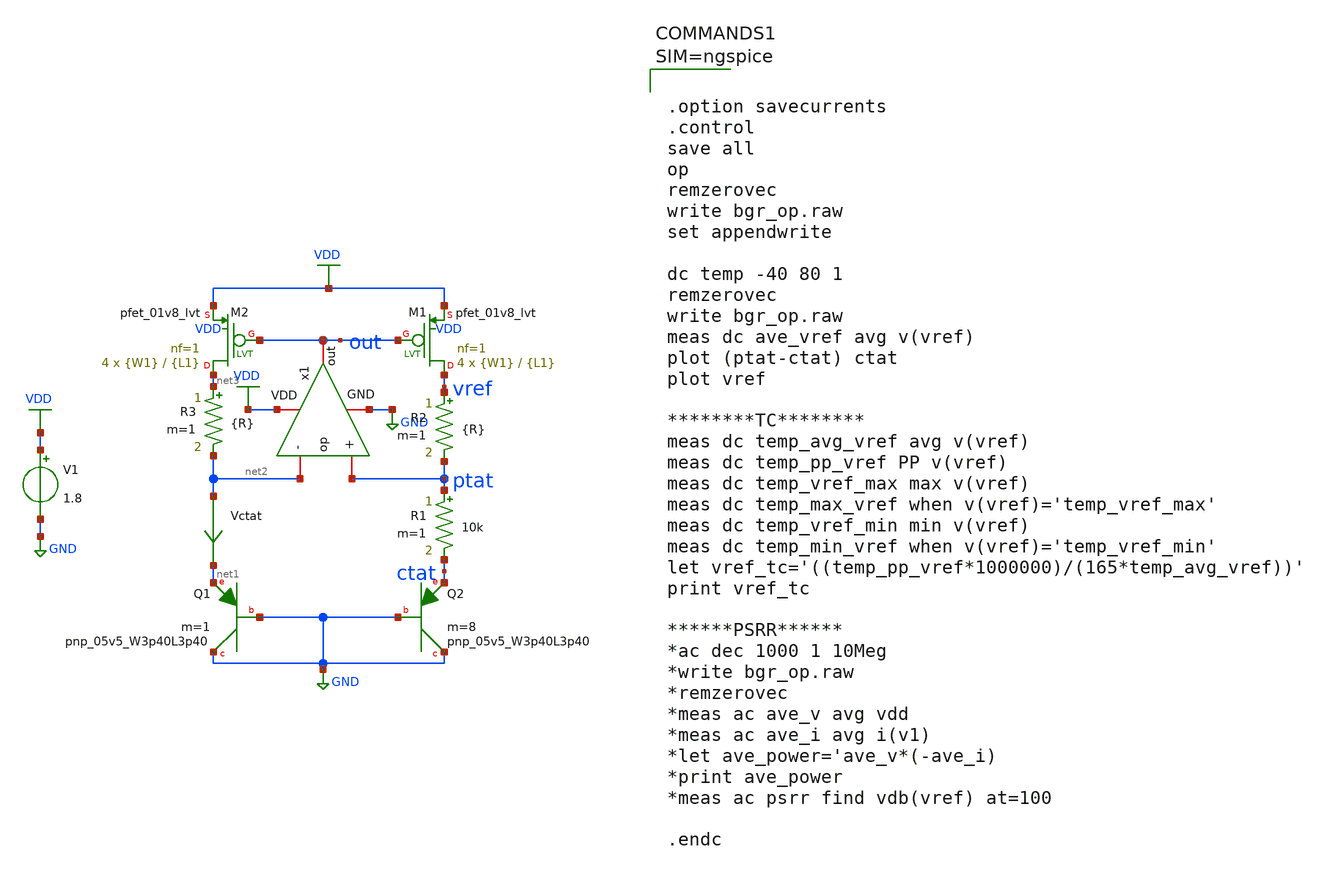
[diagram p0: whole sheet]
** sch_path: xschem/bgr_op.sch
**.subckt bgr_op
x1 VDD out net2 ptat GND op
XQ1 GND GND net1 sky130_fd_pr__pnp_05v5_W3p40L3p40 m=1
XQ2 GND GND ctat sky130_fd_pr__pnp_05v5_W3p40L3p40 m=8
R1 ptat ctat 10k m=1
XM1 vref out VDD VDD sky130_fd_pr__pfet_01v8_lvt L={L1} W={W1} nf=1 ad='int((nf+1)/2) * W/nf * 0.29'
+ as='int((nf+2)/2) * W/nf * 0.29' pd='2*int((nf+1)/2) * (W/nf + 0.29)' ps='2*int((nf+2)/2) * (W/nf + 0.29)'
+ nrd='0.29 / W' nrs='0.29 / W' sa=0 sb=0 sd=0 mult=4 m=4
XM2 net3 out VDD VDD sky130_fd_pr__pfet_01v8_lvt L={L1} W={W1} nf=1 ad='int((nf+1)/2) * W/nf * 0.29'
+ as='int((nf+2)/2) * W/nf * 0.29' pd='2*int((nf+1)/2) * (W/nf + 0.29)' ps='2*int((nf+2)/2) * (W/nf + 0.29)'
+ nrd='0.29 / W' nrs='0.29 / W' sa=0 sb=0 sd=0 mult=4 m=4
V1 VDD GND 1.8
Vctat net2 net1 0
.save i(vctat)
R2 vref ptat {R} m=1
R3 net3 net2 {R} m=1
**** begin user architecture code


.param L1=2.7
.param W1=1.5
.param R=82k



** opencircuitdesign pdks install
.lib $::SKYWATER_MODELS/sky130.lib.spice tt





.option savecurrents
.control
save all
op
remzerovec
write bgr_op.raw
set appendwrite

dc temp -40 80 1
remzerovec
write bgr_op.raw
meas dc ave_vref avg v(vref)
plot (ptat-ctat) ctat
plot vref

********TC********
meas dc temp_avg_vref avg v(vref)
meas dc temp_pp_vref PP v(vref)
meas dc temp_vref_max max v(vref)
meas dc temp_max_vref when v(vref)='temp_vref_max'
meas dc temp_vref_min min v(vref)
meas dc temp_min_vref when v(vref)='temp_vref_min'
let vref_tc='((temp_pp_vref*1000000)/(165*temp_avg_vref))'
print vref_tc

******PSRR******
*ac dec 1000 1 10Meg
*write bgr_op.raw
*remzerovec
*meas ac ave_v avg vdd
*meas ac ave_i avg i(v1)
*let ave_power='ave_v*(-ave_i)
*print ave_power
*meas ac psrr find vdb(vref) at=100

.endc



**** end user architecture code
**.ends

* expanding   symbol:  op.sym # of pins=5
** sym_path: xschem/op.sym
** sch_path: xschem/op.sch
.subckt op VDD out - + GND
*.iopin VDD
*.iopin GND
*.iopin -
*.iopin +
*.iopin out
**** begin user architecture code


.param L=2.7
.param W=1.5


**** end user architecture code
XM1 net1 net2 VDD VDD sky130_fd_pr__pfet_01v8_lvt L={L} W={W} nf=1 ad='int((nf+1)/2) * W/nf * 0.29' as='int((nf+2)/2)
+ * W/nf * 0.29' pd='2*int((nf+1)/2) * (W/nf + 0.29)' ps='2*int((nf+2)/2) * (W/nf + 0.29)' nrd='0.29 /
+ W' nrs='0.29 / W' sa=0 sb=0 sd=0 mult=4 m=4
XM2 net2 net2 VDD VDD sky130_fd_pr__pfet_01v8_lvt L={L} W={W} nf=1 ad='int((nf+1)/2) * W/nf * 0.29' as='int((nf+2)/2)
+ * W/nf * 0.29' pd='2*int((nf+1)/2) * (W/nf + 0.29)' ps='2*int((nf+2)/2) * (W/nf + 0.29)' nrd='0.29 /
+ W' nrs='0.29 / W' sa=0 sb=0 sd=0 mult=4 m=4
XM3 net1 + net3 GND sky130_fd_pr__nfet_01v8_lvt L={L} W={W} nf=1 ad='int((nf+1)/2) * W/nf * 0.29' as='int((nf+2)/2)
+ * W/nf * 0.29' pd='2*int((nf+1)/2) * (W/nf + 0.29)' ps='2*int((nf+2)/2) * (W/nf + 0.29)' nrd='0.29 /
+ W' nrs='0.29 / W' sa=0 sb=0 sd=0 mult=4 m=4
XM4 net2 - net3 GND sky130_fd_pr__nfet_01v8_lvt L={L} W={W} nf=1 ad='int((nf+1)/2) * W/nf * 0.29' as='int((nf+2)/2)
+ * W/nf * 0.29' pd='2*int((nf+1)/2) * (W/nf + 0.29)' ps='2*int((nf+2)/2) * (W/nf + 0.29)' nrd='0.29 /
+ W' nrs='0.29 / W' sa=0 sb=0 sd=0 mult=4 m=4
XM5 net3 bias GND GND sky130_fd_pr__nfet_01v8_lvt L={L} W={W} nf=1 ad='int((nf+1)/2) * W/nf * 0.29' as='int((nf+2)/2)
+ * W/nf * 0.29' pd='2*int((nf+1)/2) * (W/nf + 0.29)' ps='2*int((nf+2)/2) * (W/nf + 0.29)' nrd='0.29 /
+ W' nrs='0.29 / W' sa=0 sb=0 sd=0 mult=4 m=4
XM6 bias net4 VDD VDD sky130_fd_pr__pfet_01v8_lvt L={L*2} W={W/2} nf=1 ad='int((nf+1)/2) * W/nf * 0.29' as='int((nf+2)/2)
+ * W/nf * 0.29' pd='2*int((nf+1)/2) * (W/nf + 0.29)' ps='2*int((nf+2)/2) * (W/nf + 0.29)' nrd='0.29 /
+ W' nrs='0.29 / W' sa=0 sb=0 sd=0 mult=4 m=4
XM7 net4 net4 VDD VDD sky130_fd_pr__pfet_01v8_lvt L={L*2} W={W/2} nf=1 ad='int((nf+1)/2) * W/nf * 0.29' as='int((nf+2)/2)
+ * W/nf * 0.29' pd='2*int((nf+1)/2) * (W/nf + 0.29)' ps='2*int((nf+2)/2) * (W/nf + 0.29)' nrd='0.29 /
+ W' nrs='0.29 / W' sa=0 sb=0 sd=0 mult=4 m=4
XM8 net4 bias GND GND sky130_fd_pr__nfet_01v8_lvt L={L*2} W={W/2} nf=1 ad='int((nf+1)/2) * W/nf * 0.29' as='int((nf+2)/2)
+ * W/nf * 0.29' pd='2*int((nf+1)/2) * (W/nf + 0.29)' ps='2*int((nf+2)/2) * (W/nf + 0.29)' nrd='0.29 /
+ W' nrs='0.29 / W' sa=0 sb=0 sd=0 mult=4 m=4
XM9 bias bias GND GND sky130_fd_pr__nfet_01v8_lvt L={L*2} W={W/2} nf=1 ad='int((nf+1)/2) * W/nf * 0.29' as='int((nf+2)/2)
+ * W/nf * 0.29' pd='2*int((nf+1)/2) * (W/nf + 0.29)' ps='2*int((nf+2)/2) * (W/nf + 0.29)' nrd='0.29 /
+ W' nrs='0.29 / W' sa=0 sb=0 sd=0 mult=4 m=4
XM10 out bias GND GND sky130_fd_pr__nfet_01v8_lvt L={L} W={W/2} nf=1 ad='int((nf+1)/2) * W/nf * 0.29' as='int((nf+2)/2)
+ * W/nf * 0.29' pd='2*int((nf+1)/2) * (W/nf + 0.29)' ps='2*int((nf+2)/2) * (W/nf + 0.29)' nrd='0.29 /
+ W' nrs='0.29 / W' sa=0 sb=0 sd=0 mult=4 m=4
XM11 out net1 VDD VDD sky130_fd_pr__pfet_01v8_lvt L={L} W={W} nf=1 ad='int((nf+1)/2) * W/nf * 0.29' as='int((nf+2)/2)
+ * W/nf * 0.29' pd='2*int((nf+1)/2) * (W/nf + 0.29)' ps='2*int((nf+2)/2) * (W/nf + 0.29)' nrd='0.29 /
+ W' nrs='0.29 / W' sa=0 sb=0 sd=0 mult=4 m=4
C2 out net5 1p m=1
R2 net5 net1 40k m=1
.ends

.GLOBAL VDD
.GLOBAL GND
.end
